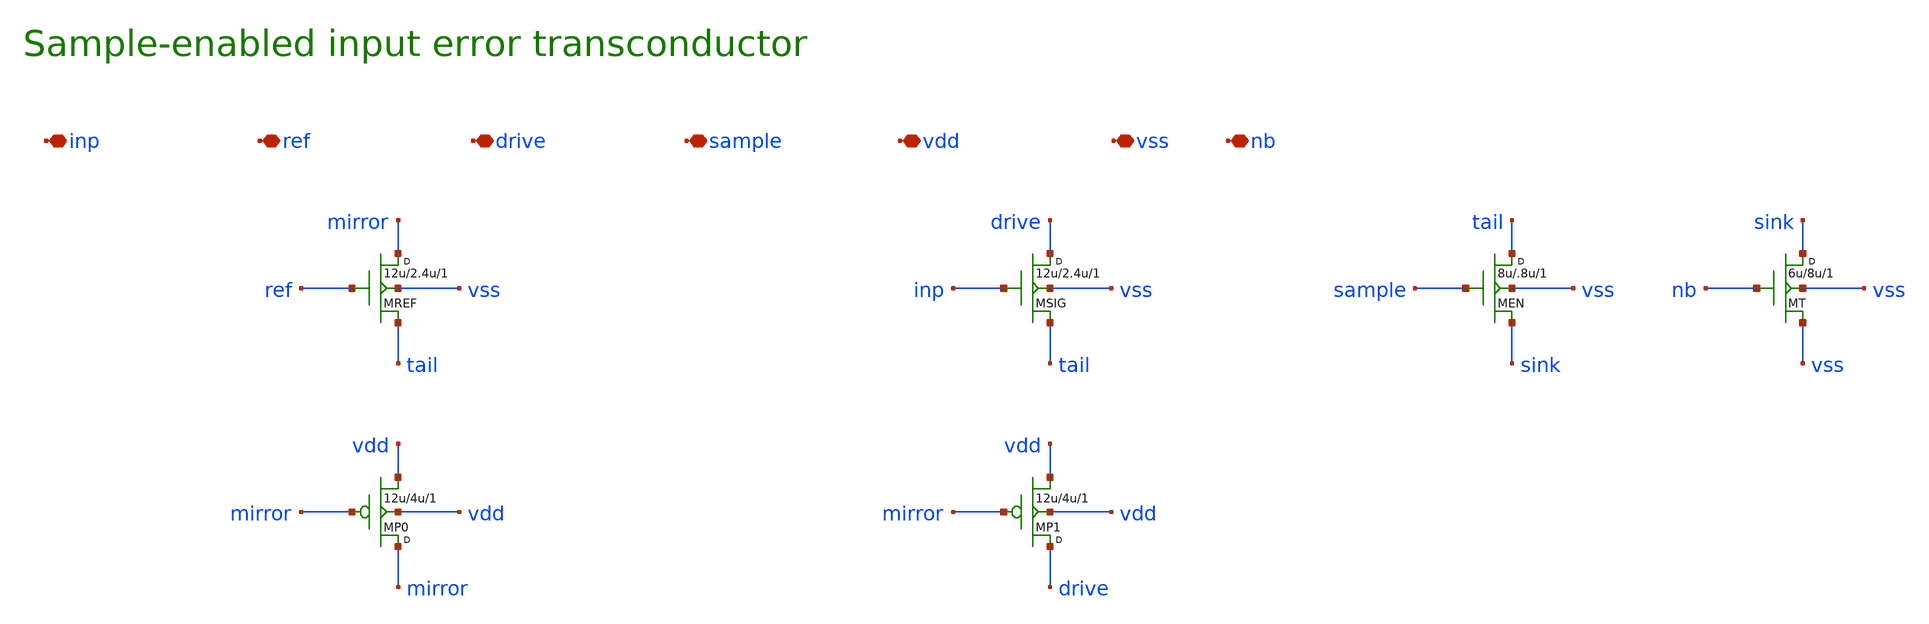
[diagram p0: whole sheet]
** sch_path: ICMC/schematic/icm_error08.sch
**.subckt icm_error08 inp ref drive sample vdd vss nb
*.iopin inp
*.iopin ref
*.iopin drive
*.iopin sample
*.iopin vdd
*.iopin vss
*.iopin nb
MREF mirror ref tail vss N w=12u l=2.4u m=1
MSIG drive inp tail vss N w=12u l=2.4u m=1
MEN tail sample sink vss N w=8u l=.8u m=1
MT sink nb vss vss N w=6u l=8u m=1
MP0 mirror mirror vdd vdd P w=12u l=4u m=1
MP1 drive mirror vdd vdd P w=12u l=4u m=1
**.ends
.end
